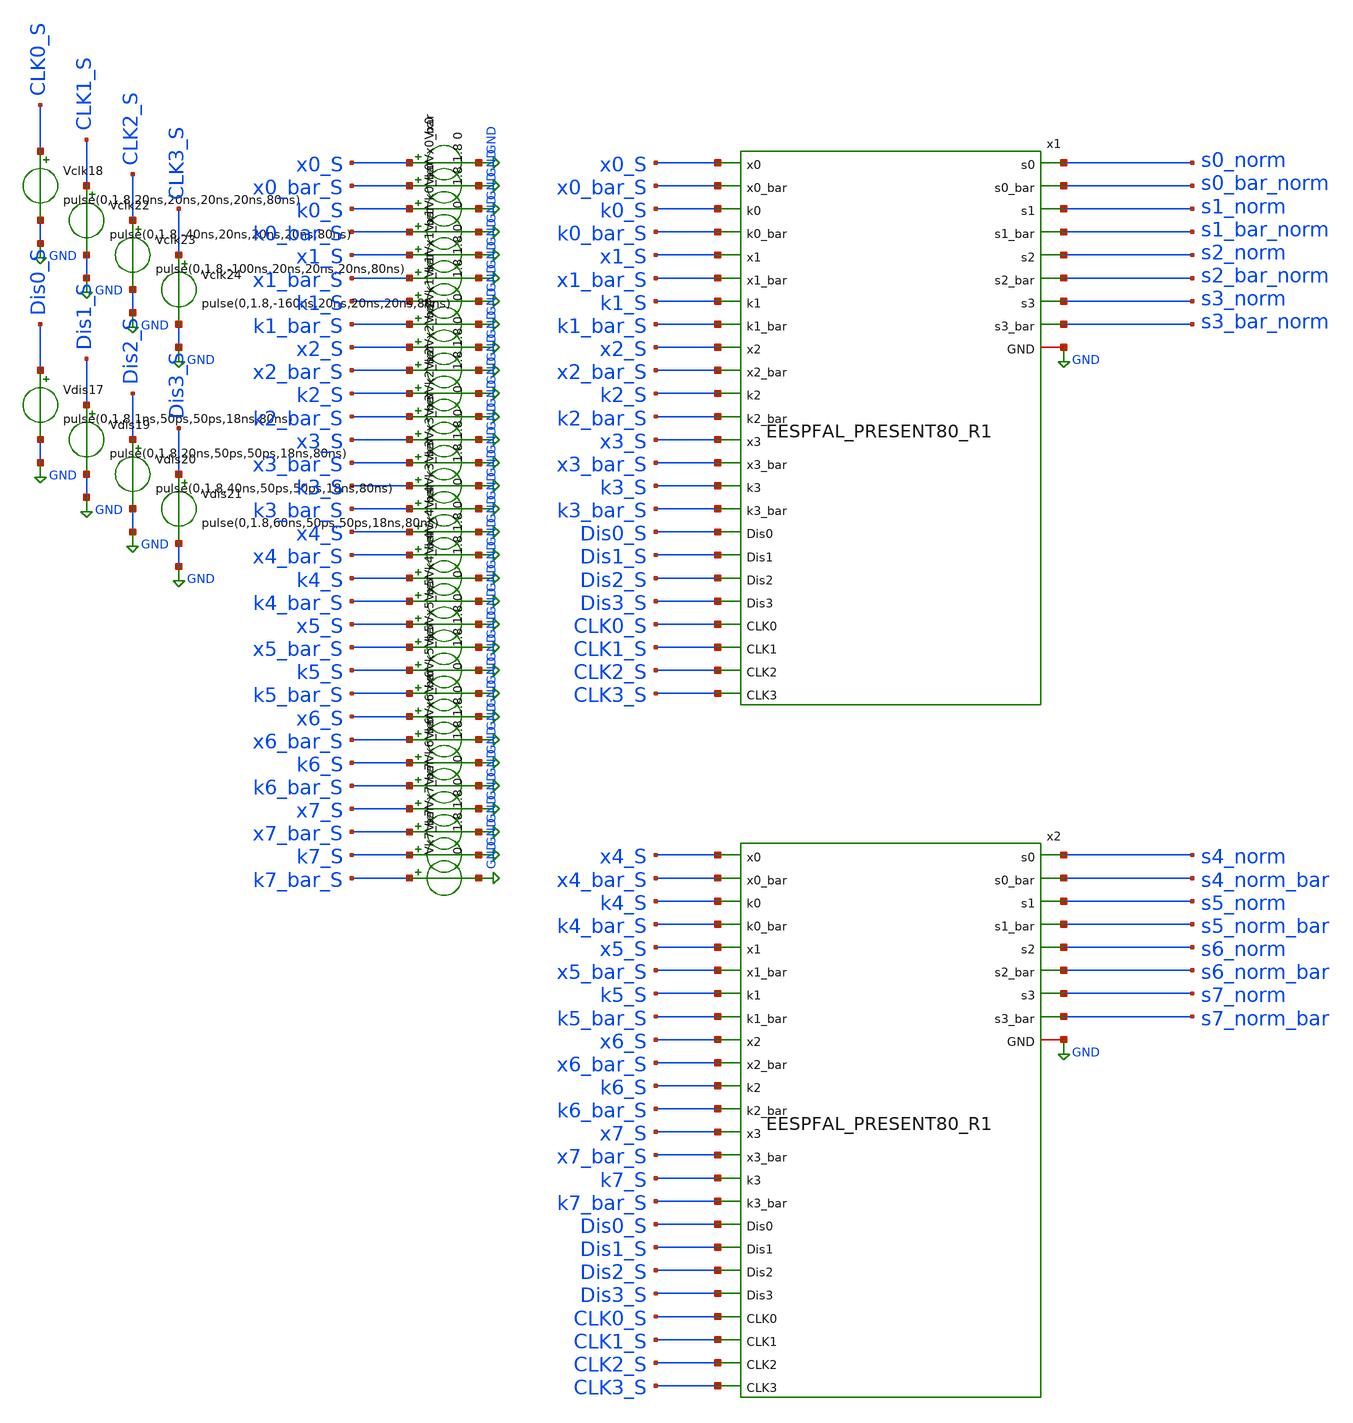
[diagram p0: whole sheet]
** sch_path: skywater_stuff/untitled-25.sch
**.subckt untitled-25
Vdis17 Dis0_S GND pulse(0,1.8,1ns,50ps,50ps,18ns,80ns)
Vclk18 CLK0_S GND pulse(0,1.8,20ns,20ns,20ns,20ns,80ns)
Vdis19 Dis1_S GND pulse(0,1.8,20ns,50ps,50ps,18ns,80ns)
Vdis20 Dis2_S GND pulse(0,1.8,40ns,50ps,50ps,18ns,80ns)
Vdis21 Dis3_S GND pulse(0,1.8,60ns,50ps,50ps,18ns,80ns)
Vclk22 CLK1_S GND pulse(0,1.8,-40ns,20ns,20ns,20ns,80ns)
Vclk23 CLK2_S GND pulse(0,1.8,-100ns,20ns,20ns,20ns,80ns)
Vclk24 CLK3_S GND pulse(0,1.8,-160ns,20ns,20ns,20ns,80ns)
Vx0 x0_S GND 0
Vx0_bar x0_bar_S GND 1.8
Vk0 k0_S GND 1.8
Vk0_bar k0_bar_S GND 0
Vx1 x1_S GND 0
Vx1_bar x1_bar_S GND 1.8
Vk1 k1_S GND 1.8
Vk1_bar k1_bar_S GND 0
Vx2 x2_S GND 0
Vx2_bar x2_bar_S GND 1.8
Vk2 k2_S GND 1.8
Vk2_bar k2_bar_S GND 0
Vx3 x3_S GND 0
Vx3_bar x3_bar_S GND 1.8
Vk3 k3_S GND 1.8
Vk3_bar k3_bar_S GND 0
Vx4 x4_S GND 0
Vx4_bar x4_bar_S GND 1.8
Vk4 k4_S GND 1.8
Vk4_bar k4_bar_S GND 0
Vx5 x5_S GND 0
Vx5_bar x5_bar_S GND 1.8
Vk5 k5_S GND 1.8
Vk5_bar k5_bar_S GND 0
Vx6 x6_S GND 0
Vx6_bar x6_bar_S GND 1.8
Vk6 k6_S GND 1.8
Vk6_bar k6_bar_S GND 0
Vx7 x7_S GND 0
Vx7_bar x7_bar_S GND 1.8
Vk7 k7_S GND 1.8
Vk7_bar k7_bar_S GND 0
x1 GND x0_S x0_bar_S k0_S k0_bar_S x1_S x1_bar_S k1_S k1_bar_S x2_S x2_bar_S k2_S k2_bar_S x3_S
+ x3_bar_S k3_S k3_bar_S s0_norm s0_bar_norm CLK0_S Dis0_S CLK1_S Dis1_S s2_norm s2_bar_norm s3_bar_norm
+ s3_norm s1_bar_norm s1_norm CLK3_S Dis2_S CLK2_S Dis3_S EESPFAL_PRESENT80_R1
x2 GND x4_S x4_bar_S k4_S k4_bar_S x5_S x5_bar_S k5_S k5_bar_S x6_S x6_bar_S k6_S k6_bar_S x7_S
+ x7_bar_S k7_S k7_bar_S s4_norm s4_norm_bar CLK0_S Dis0_S CLK1_S Dis1_S s6_norm s6_norm_bar s7_norm_bar
+ s7_norm s5_norm_bar s5_norm CLK3_S Dis2_S CLK2_S Dis3_S EESPFAL_PRESENT80_R1
**** begin user architecture code

.lib /research/pdk/open_pdks/share/pdk/sky130A/libs.tech/ngspice/sky130.lib.spice tt
**.include ~/magic_layout_stuff/EESPFAL_PRESENT80_R1.spice
**.include ~/magic_layout_stuff/EESPFAL_PRESENT80_R1_flat.spice
.param v0 ='0' v0_bar ='1.8' v1 ='0' v1_bar ='1.8' v2 ='0' v2_bar ='1.8' v3 ='0' v3_bar ='1.8'
.option method=gear
.control
echo We at start now
set tstart=0
*set tstop=0
let index=0
let index2=1
let wstart = $tstart
let wstop = 0n
let key = 7
let total_time = 32
let cycle_index = 800

*foreach bit_index 0 1 2 3
*	set bit = `./test.sh $&key $bit_index`
*	alter Vk$bit_index = '$bit ? 1.8 : 0'
*	alter Vk`echo $bit_index`_bar = '$bit ? 0 : 1.8'
*end

let bit_index = 0
while bit_index < 8
	set bit = `./test.sh $&key $&bit_index`
	alter Vk$&bit_index = '$bit ? 1.8 : 0'
	alter Vk`echo $&bit_index`_bar = '$bit ? 0 : 1.8'
	let bit_index = bit_index + 1
end

set values_raw < circ_inputs_`echo $&cycle_index`.txt
*set values_raw < circ_inputs_not_rand_`echo $&cycle_index`.txt
compose values values $values_raw
echo stuff

*let curr_time = index*80n

while index2 < length(values)
	let wstop = $&index2*80n
	stop when time=$&wstop
	let index2 = $&index2+1
	echo $&index2
end

let tstop = length(values)*80n
while index < length(values)
	let value = values[$&index]
	echo $&value
	echo going into altering
	let bit_index = 0
	while bit_index < 64
		set bit = `./test.sh $&value $&bit_index`
		alter Vx$&bit_index = '$bit ? 1.8 : 0'
		alter Vx`echo $&bit_index`_bar = '$bit ? 0 : 1.8'
		let bit_index = bit_index + 1
	end
	echo test stuff
	let index=index+1
	if index = 1
		tran 1n $&tstop 0 1n
	else
		resume
	end
end

*let Pinst_CLK0_CLK3 =
*+ (v(CLK0_S)*i(vclk18))+(v(CLK1_S)*i(vclk22))+(v(CLK2_S)*i(vclk23))+(v(CLK3_S)*i(vclk24))
*plot Pinst_CLK0_CLK3
let index = 0
while index < length(values)
	let Pinst_CLK0_CLK3 =
+ (v(CLK0_S)*i(vclk18))+(v(CLK1_S)*i(vclk22))+(v(CLK2_S)*i(vclk23))+(v(CLK3_S)*i(vclk24))
	**let Pinst_CLK0_CLK3_Dis0_Dis3 =
+ (v(CLK0_S)*i(vclk18))+(v(CLK1_S)*i(vclk22))+(v(CLK2_S)*i(vclk23))+(v(CLK3_S)*i(vclk24))+(v(Dis0_S)*i(vdis17))+(v(Dis1_S)*i(vdis19))+(v(Dis2_S)*i(vdis20))+(v(Dis3_S)*i(vdis21))
	**plot Pinst_CLK0_CLK3
	let lin-tstart = $&index*80ns
	let lin-tstop = $&lin-tstart+80ns
	let lin-tstep = 0.1n
	linearize Pinst_CLK0_CLK3
	*display
	set appendwrite
	*wrdata EESPFAL_K`echo $&key`_`echo $&total_time`u_`echo $&cycle_index`cycle_norm.csv
+ Pinst_CLK0_CLK3
	*wrdata EESPFAL_FULL_R1_K`echo $&key`_`echo $&total_time`u_`echo $&cycle_index`cycle_norm.csv
+ Pinst_CLK0_CLK3
	wrdata EESPFAL_32bits_K`echo $&key`_`echo $&total_time`u_`echo $&cycle_index`cycle_norm.csv
+ Pinst_CLK0_CLK3
	*wrdata EESPFAL_K`echo $&key`_`echo $&total_time`u_`echo $&cycle_index`cycle_flat.csv
+ Pinst_CLK0_CLK3
	let index = index + 1
	*echo $plots
	setplot tran1
	destroy tran2
	*echo $plots
end
.endc


**** end user architecture code
**.ends
.GLOBAL GND
.end
